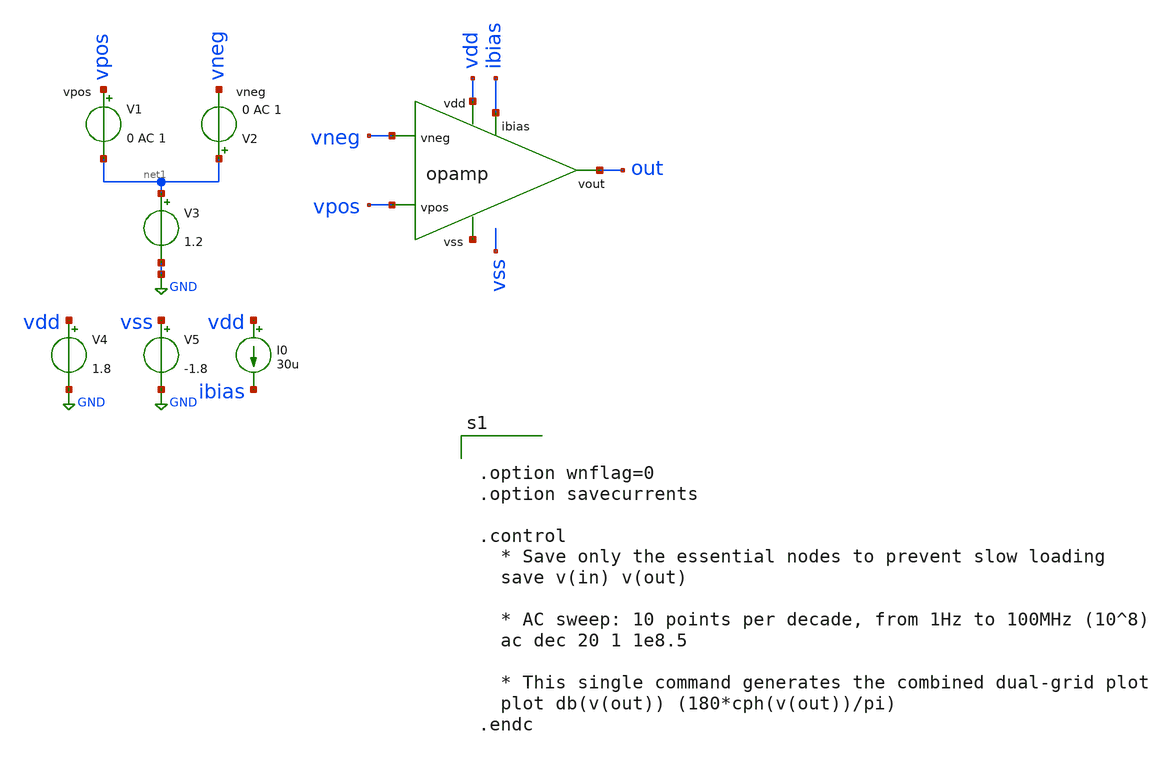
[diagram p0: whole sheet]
** sch_path: sch/opamp_tb.sch
**.subckt opamp_tb
V1 vpos net1 0 AC 1
V2 net1 vneg 0 AC 1
V3 net1 GND 1.2
V4 vdd GND 1.8
V5 vss GND -1.8
I0 vdd ibias 30u
x1 vdd net2 vneg vpos out ibias opamp
**** begin user architecture code


.option wnflag=0
.option savecurrents

.control
  * Save only the essential nodes to prevent slow loading
  save v(in) v(out)

  * AC sweep: 10 points per decade, from 1Hz to 100MHz (10^8)
  ac dec 20 1 1e8.5

  * This single command generates the combined dual-grid plot
  plot db(v(out)) (180*cph(v(out))/pi)
.endc




.lib /foss/pdks/sky130A/libs.tech/ngspice/sky130.lib.spice tt

.param mc_mm_switch=0
.param mc_pr_switch=1


**** end user architecture code
**.ends
.GLOBAL GND
.end
